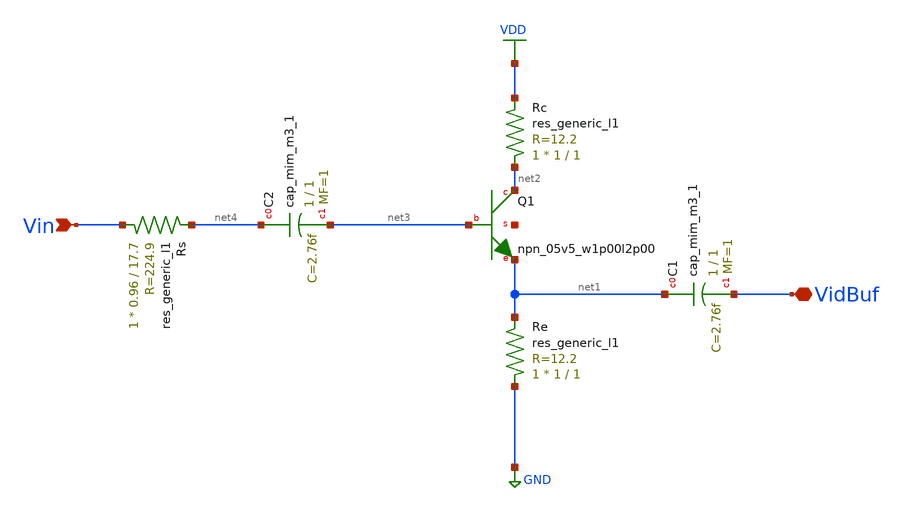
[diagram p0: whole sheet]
** sch_path: xschem/analog_desing/Buffer.sch
**.subckt Buffer VidBuf Vin
*.iopin VidBuf
*.ipin Vin
XQ1 net2 net3 net1 net5 sky130_fd_pr__npn_05v5_w1p00l2p00
XC1 net1 VidBuf sky130_fd_pr__cap_mim_m3_1 W=1 L=1 MF=1 m=1
Re GND net1 sky130_fd_pr__res_generic_l1 W=1 L=1 m=1
Rc net2 VDD sky130_fd_pr__res_generic_l1 W=1 L=1 m=1
XC2 net4 net3 sky130_fd_pr__cap_mim_m3_1 W=1 L=1 MF=1 m=1
Rs Vin net4 sky130_fd_pr__res_generic_l1 W=0.96 L=17.7 m=1
**.ends
.GLOBAL VDD
.GLOBAL GND
.end
